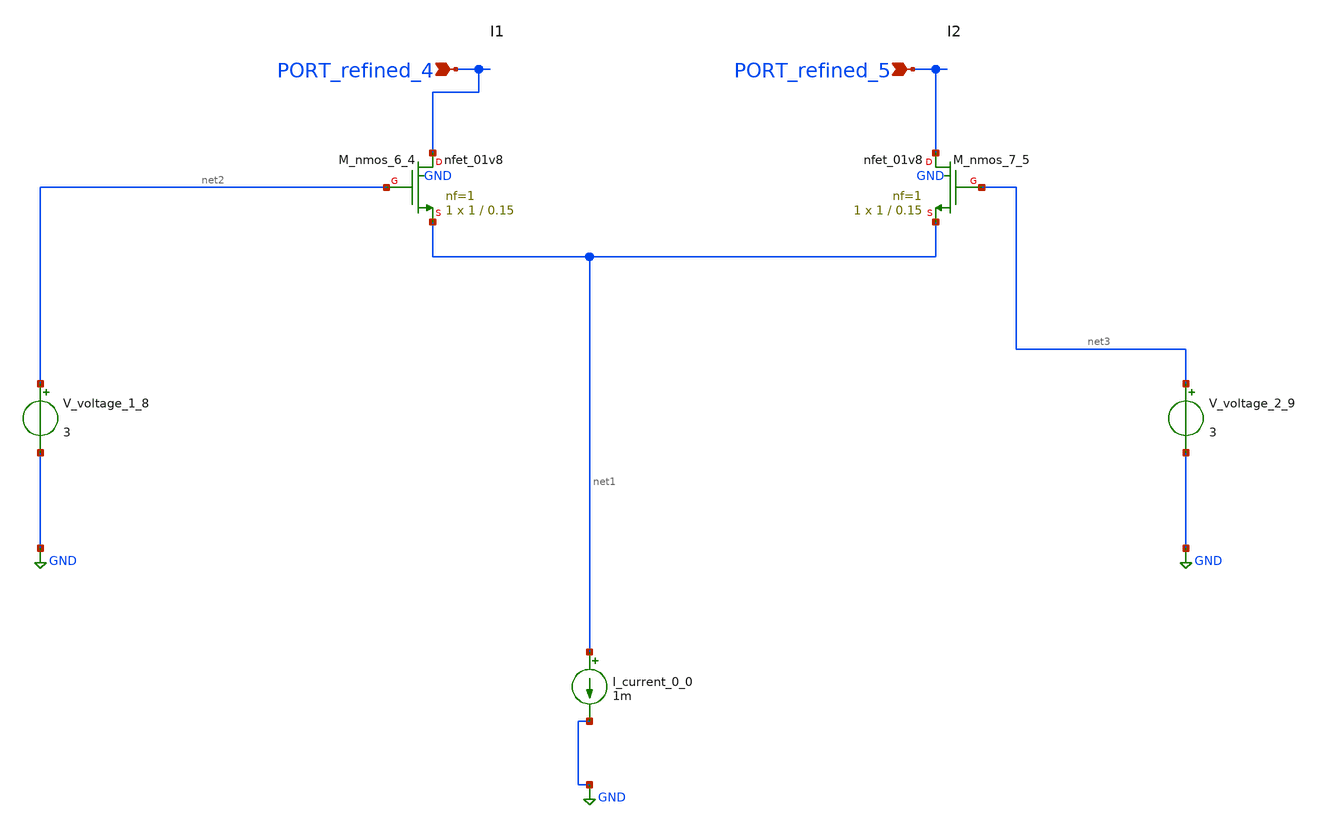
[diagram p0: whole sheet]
** sch_path: schematics/AMSNet/202.sch
**.subckt 202 PORT_refined_4 PORT_refined_5
*.ipin PORT_refined_4
*.ipin PORT_refined_5
I_current_0_0 net1 GND 1m
XM_nmos_6_4 PORT_refined_4 net2 net1 GND sky130_fd_pr__nfet_01v8 L=0.15 W=1 nf=1 ad='int((1 + 1)/2) * 1 / 1 * 0.29'
+ as='int((1 + 2)/2) * 1 / 1 * 0.29' pd='2*int((1 + 1)/2) * (1 / 1 + 0.29)' ps='2*int((1 + 2)/2) * (1 / 1 + 0.29)'
+ nrd='0.29 / 1 ' nrs='0.29 / 1 ' sa=0 sb=0 sd=0 mult=1 m=1
XM_nmos_7_5 PORT_refined_5 net3 net1 GND sky130_fd_pr__nfet_01v8 L=0.15 W=1 nf=1 ad='int((1 + 1)/2) * 1 / 1 * 0.29'
+ as='int((1 + 2)/2) * 1 / 1 * 0.29' pd='2*int((1 + 1)/2) * (1 / 1 + 0.29)' ps='2*int((1 + 2)/2) * (1 / 1 + 0.29)'
+ nrd='0.29 / 1 ' nrs='0.29 / 1 ' sa=0 sb=0 sd=0 mult=1 m=1
V_voltage_1_8 net2 GND 3
V_voltage_2_9 net3 GND 3
**.ends
.GLOBAL GND
.end
